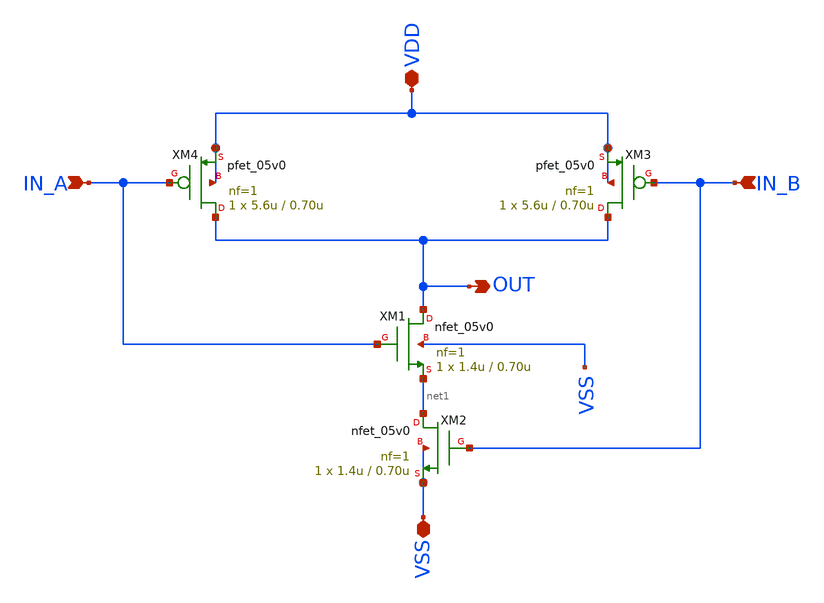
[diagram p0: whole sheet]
** sch_path: design/schematics/NOCG/SG_B11_cic_bms_afe_nand.sch
**.subckt SG_B11_cic_bms_afe_nand VDD IN_A IN_B OUT VSS
*.iopin VDD
*.ipin IN_A
*.ipin IN_B
*.opin OUT
*.iopin VSS
XM1 OUT IN_A net1 VSS nfet_05v0 L=0.70u W=1.4u nf=1 ad='int((nf+1)/2) * W/nf * 0.18u' as='int((nf+2)/2) * W/nf * 0.18u'
+ pd='2*int((nf+1)/2) * (W/nf + 0.18u)' ps='2*int((nf+2)/2) * (W/nf + 0.18u)' nrd='0.18u / W' nrs='0.18u / W'
+ sa=0 sb=0 sd=0 m=1
XM2 net1 IN_B VSS VSS nfet_05v0 L=0.70u W=1.4u nf=1 ad='int((nf+1)/2) * W/nf * 0.18u' as='int((nf+2)/2) * W/nf * 0.18u'
+ pd='2*int((nf+1)/2) * (W/nf + 0.18u)' ps='2*int((nf+2)/2) * (W/nf + 0.18u)' nrd='0.18u / W' nrs='0.18u / W'
+ sa=0 sb=0 sd=0 m=1
XM3 OUT IN_B VDD VDD pfet_05v0 L=0.70u W=5.6u nf=1 ad='int((nf+1)/2) * W/nf * 0.18u' as='int((nf+2)/2) * W/nf * 0.18u'
+ pd='2*int((nf+1)/2) * (W/nf + 0.18u)' ps='2*int((nf+2)/2) * (W/nf + 0.18u)' nrd='0.18u / W' nrs='0.18u / W'
+ sa=0 sb=0 sd=0 m=1
XM4 OUT IN_A VDD VDD pfet_05v0 L=0.70u W=5.6u nf=1 ad='int((nf+1)/2) * W/nf * 0.18u' as='int((nf+2)/2) * W/nf * 0.18u'
+ pd='2*int((nf+1)/2) * (W/nf + 0.18u)' ps='2*int((nf+2)/2) * (W/nf + 0.18u)' nrd='0.18u / W' nrs='0.18u / W'
+ sa=0 sb=0 sd=0 m=1
**.ends
.end
